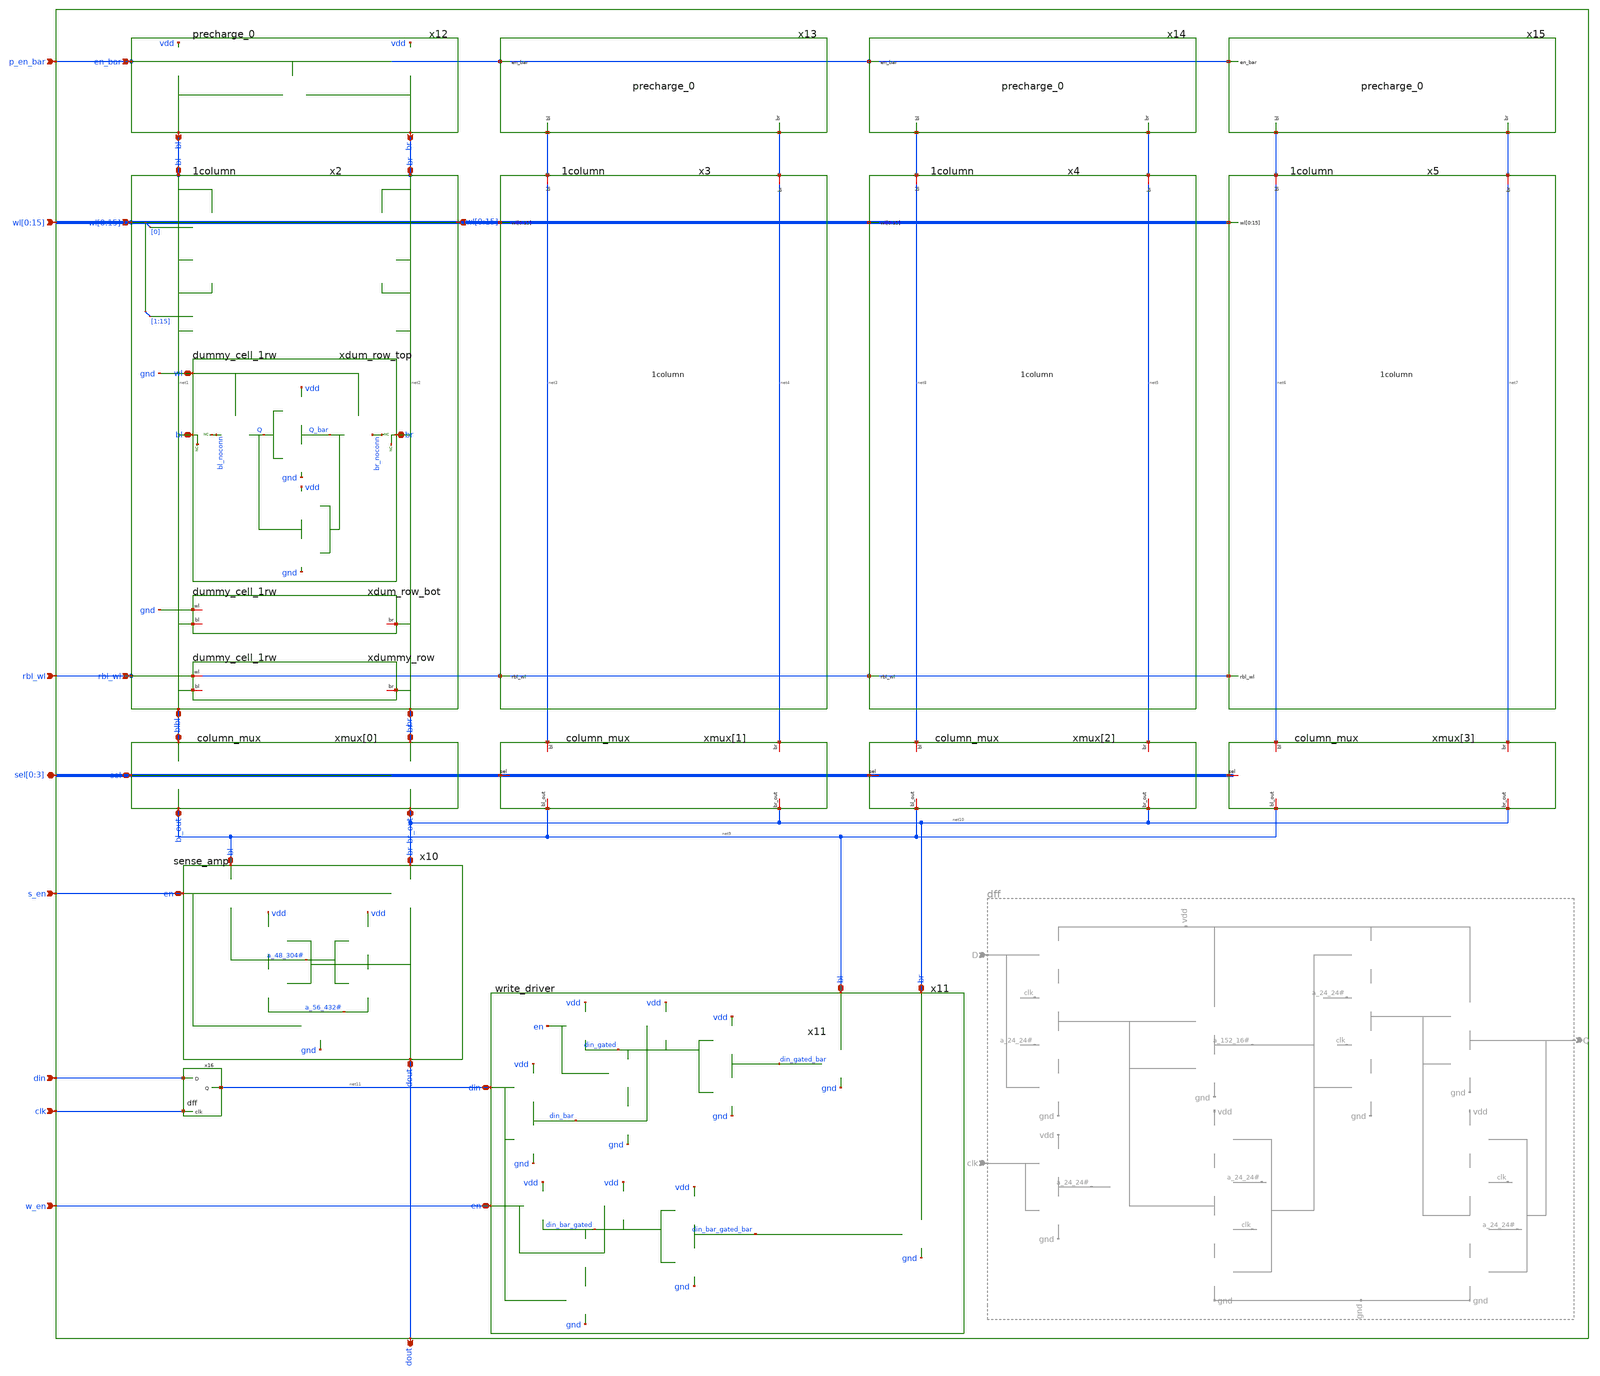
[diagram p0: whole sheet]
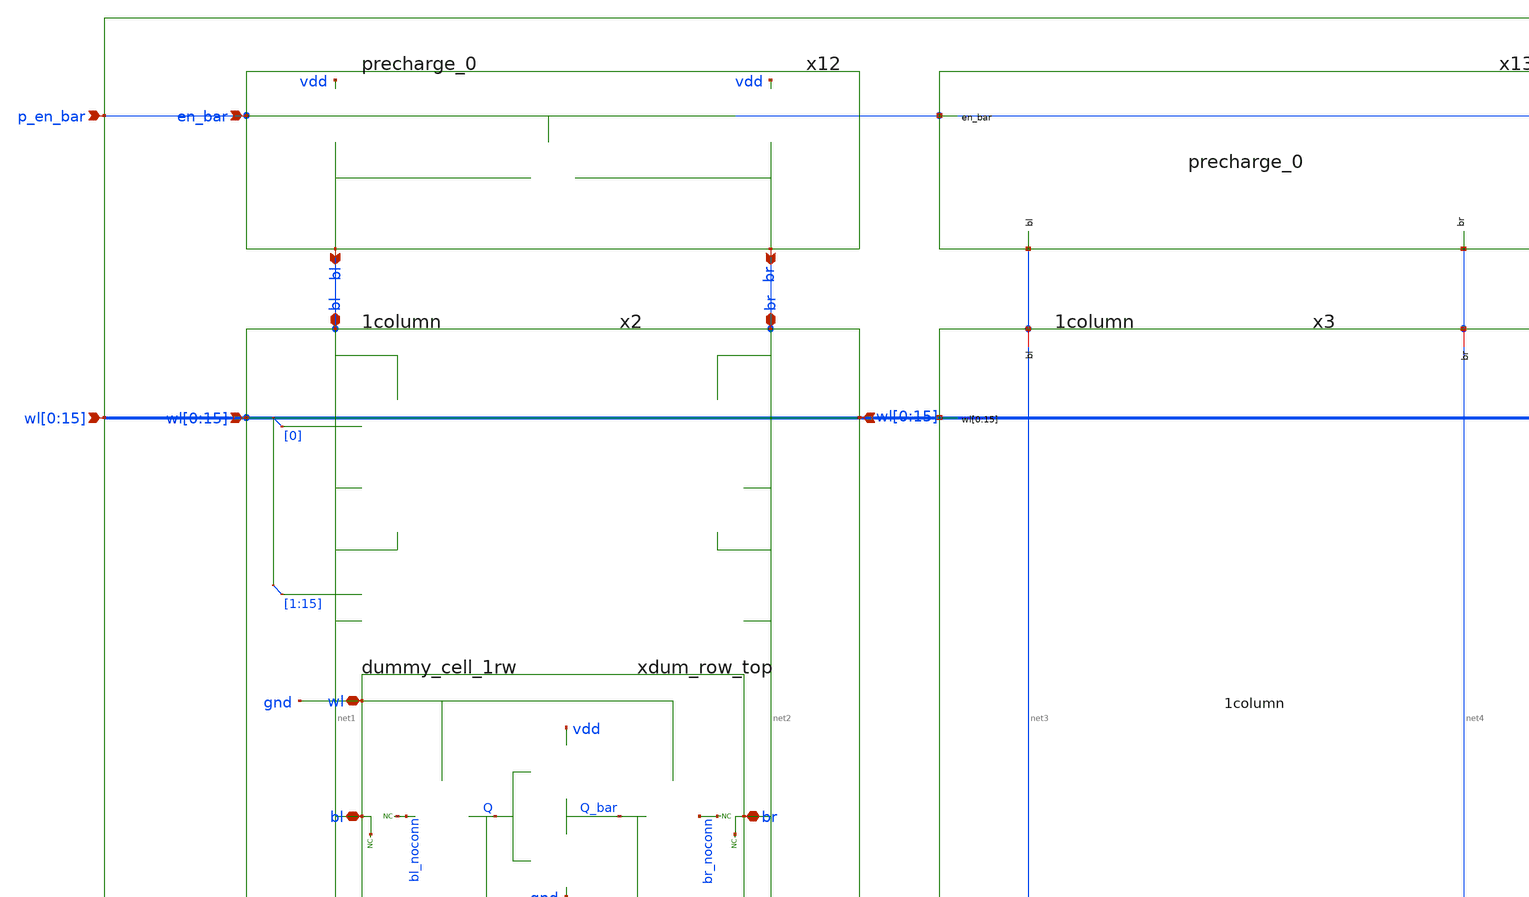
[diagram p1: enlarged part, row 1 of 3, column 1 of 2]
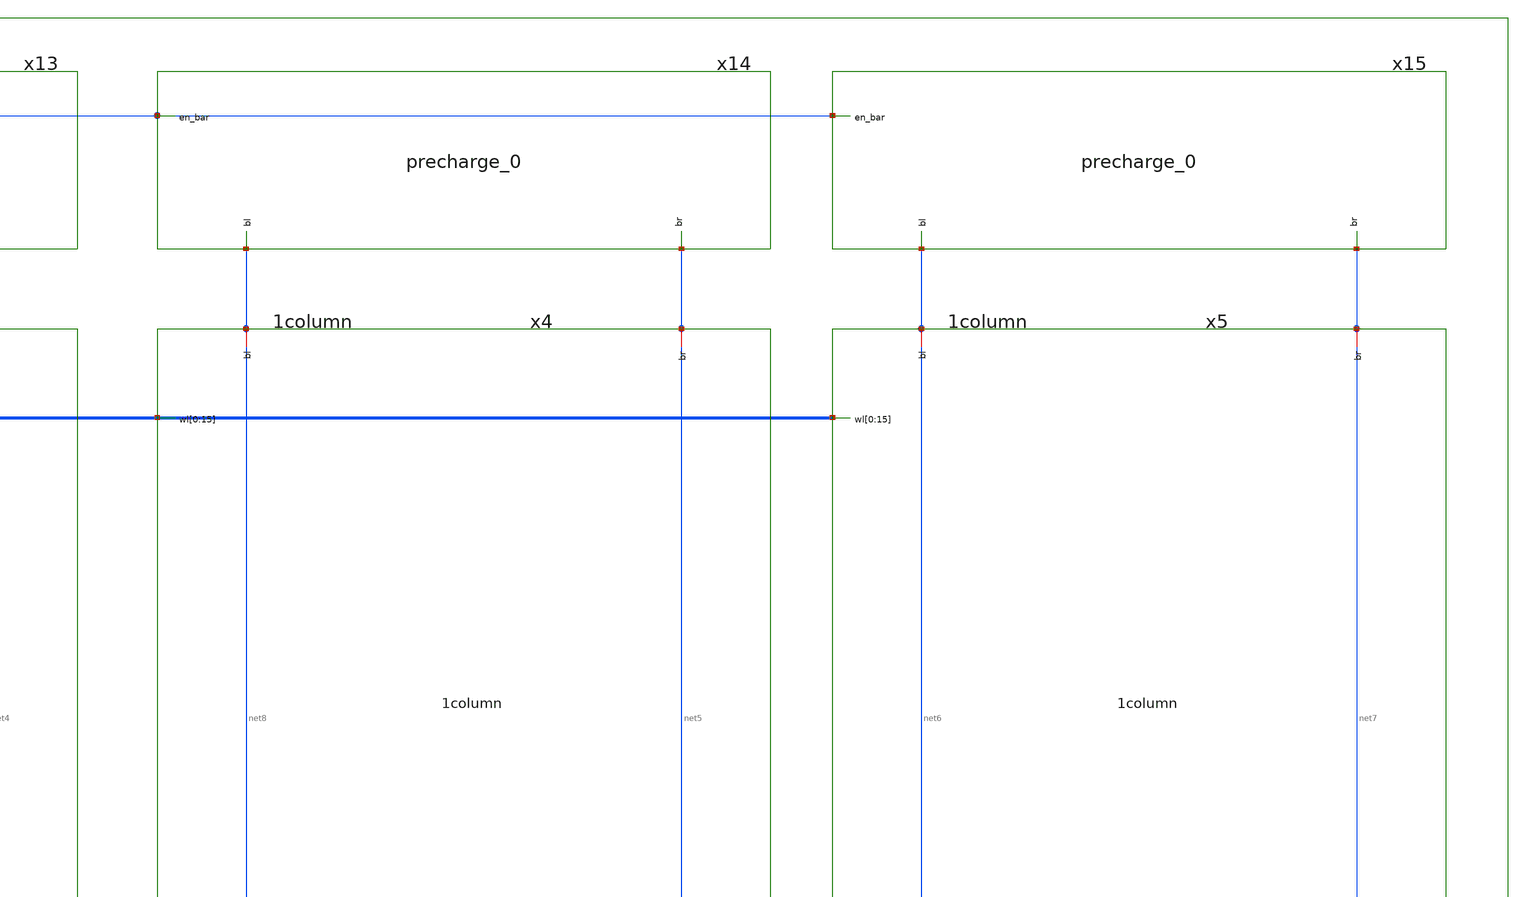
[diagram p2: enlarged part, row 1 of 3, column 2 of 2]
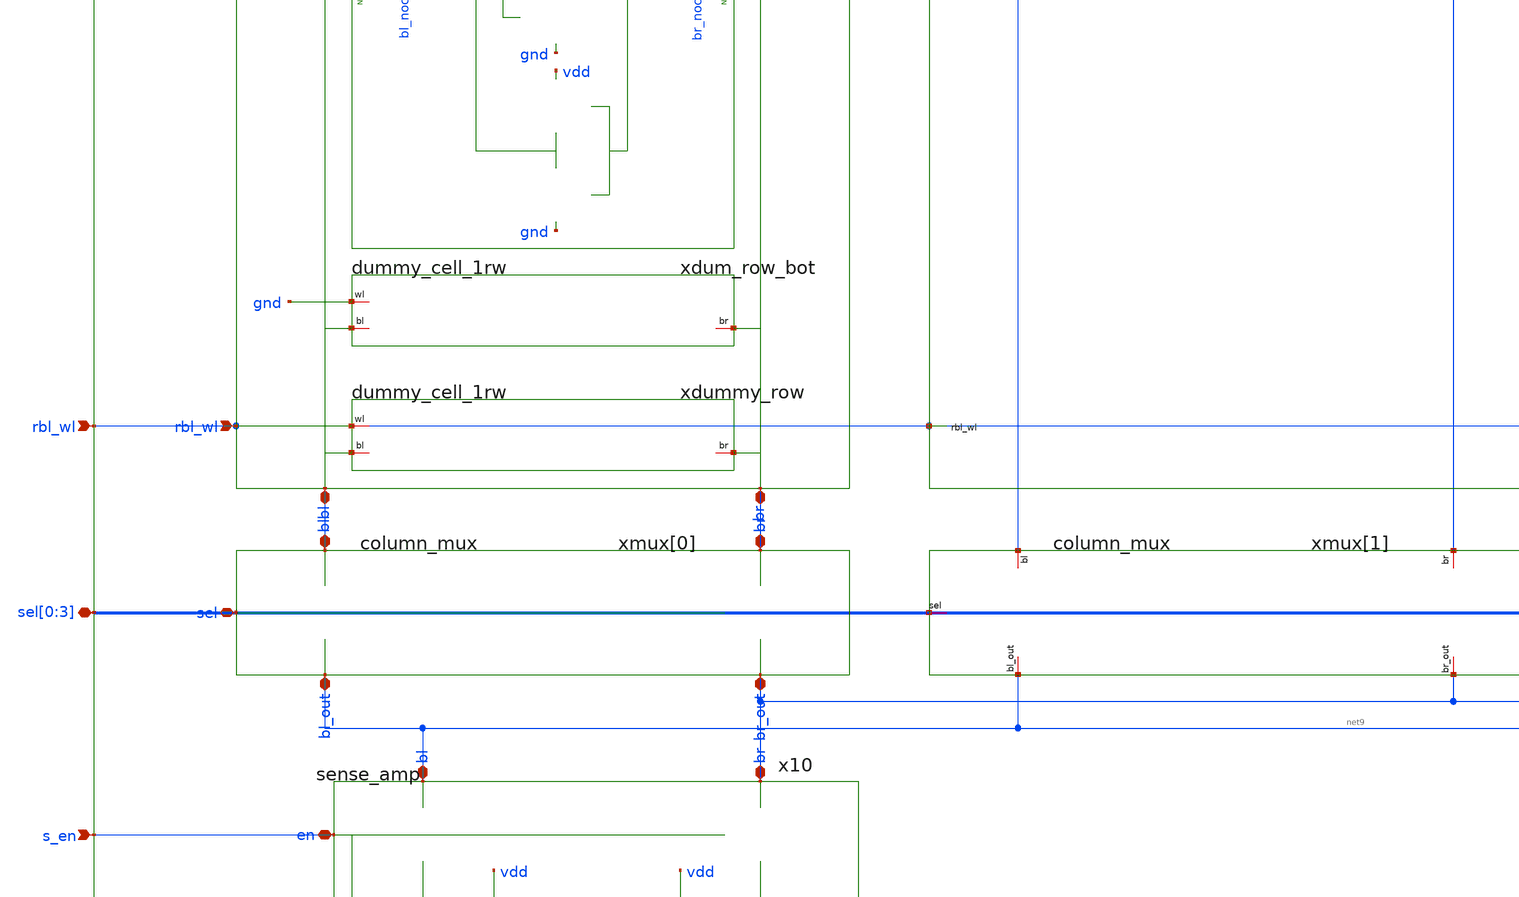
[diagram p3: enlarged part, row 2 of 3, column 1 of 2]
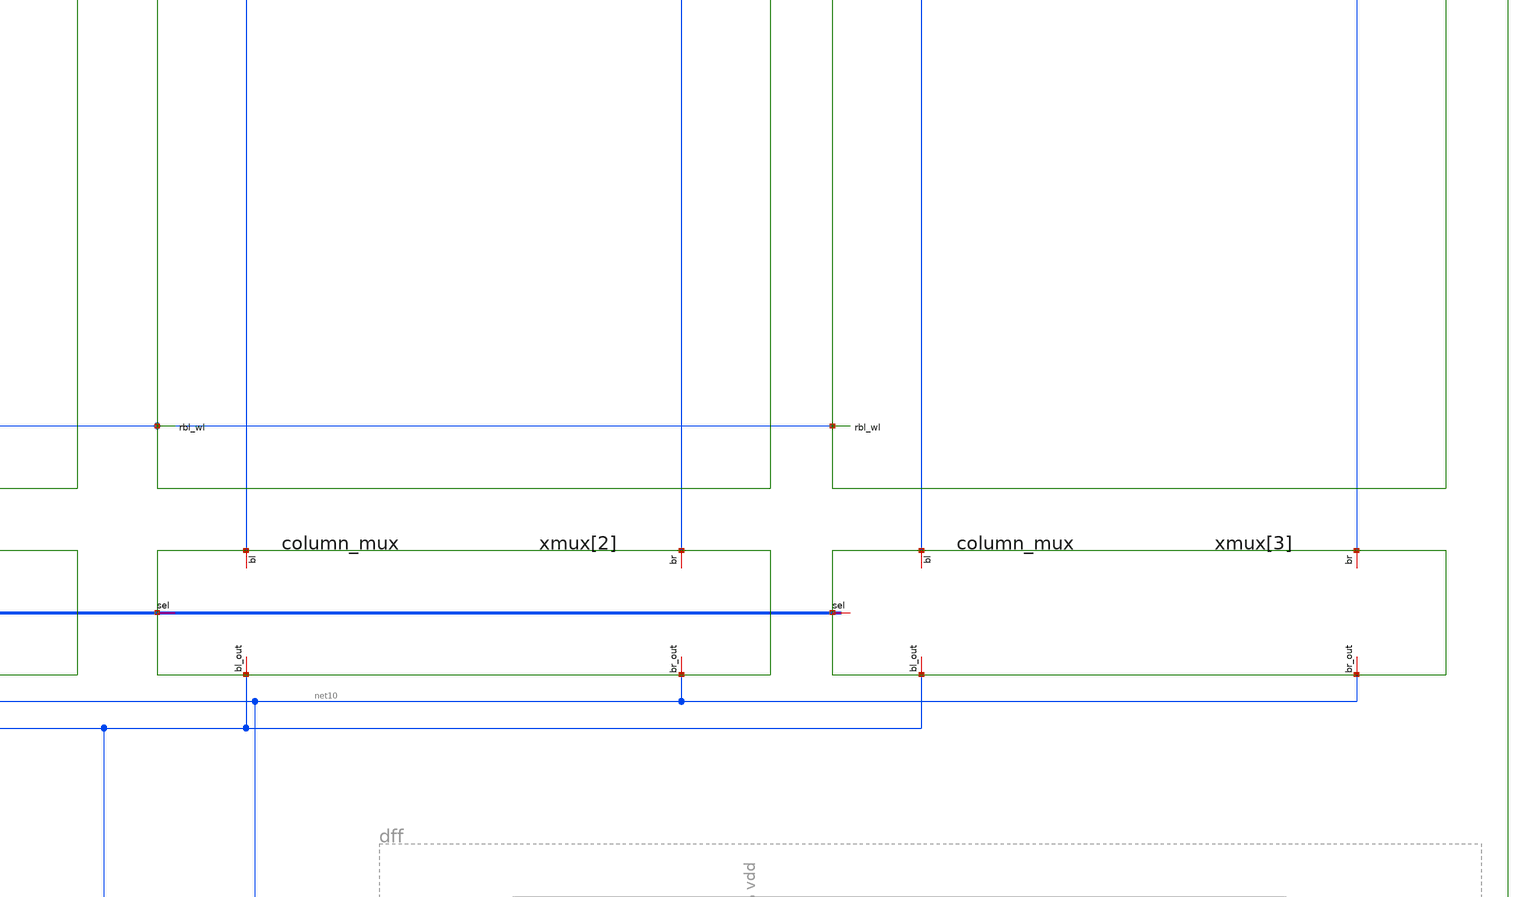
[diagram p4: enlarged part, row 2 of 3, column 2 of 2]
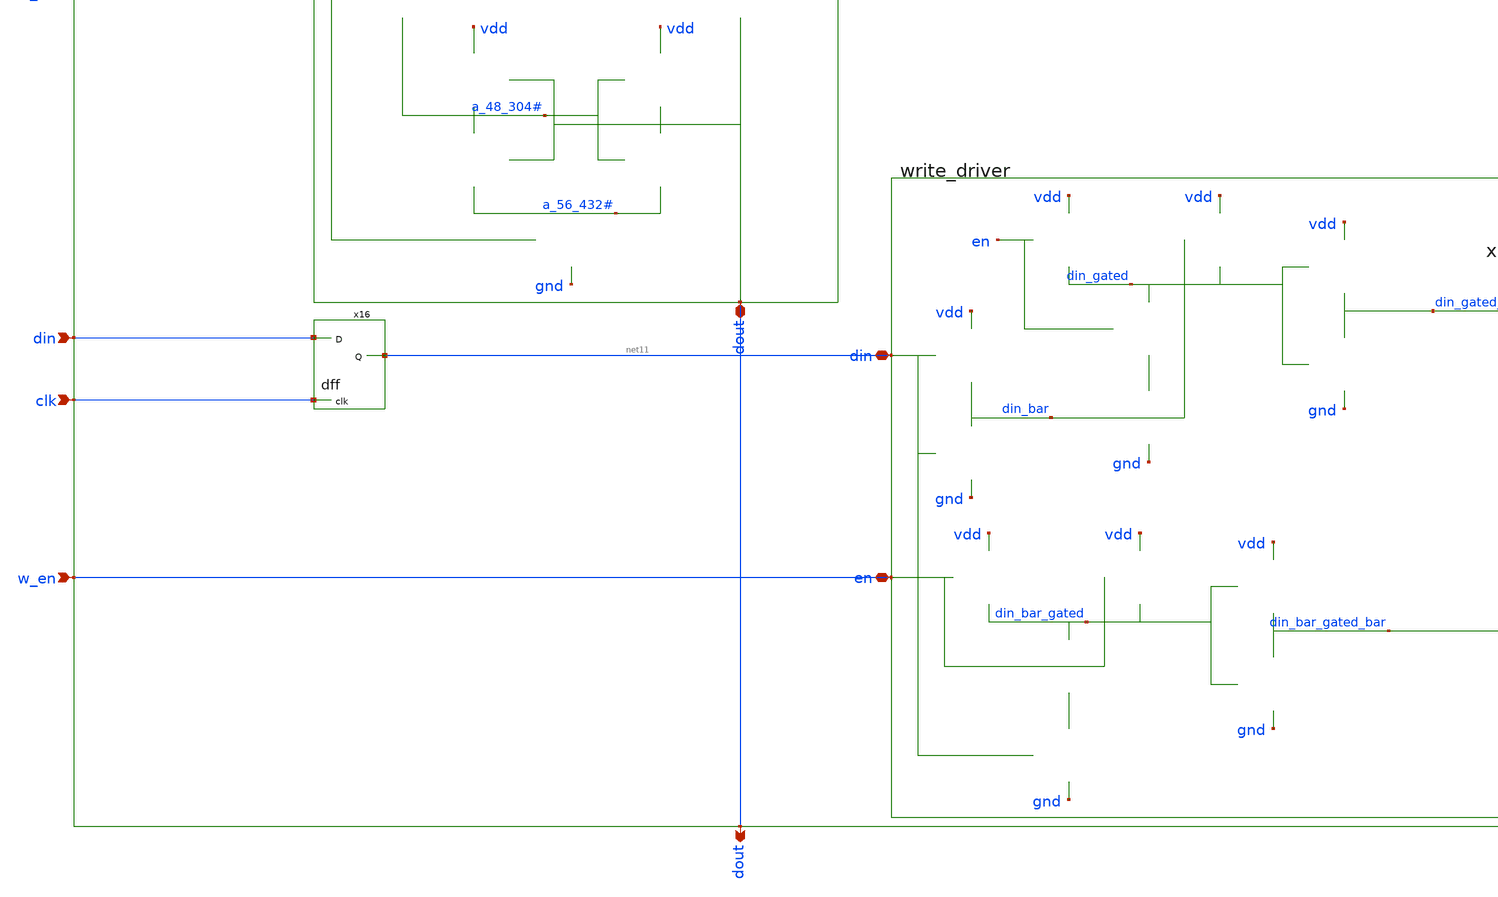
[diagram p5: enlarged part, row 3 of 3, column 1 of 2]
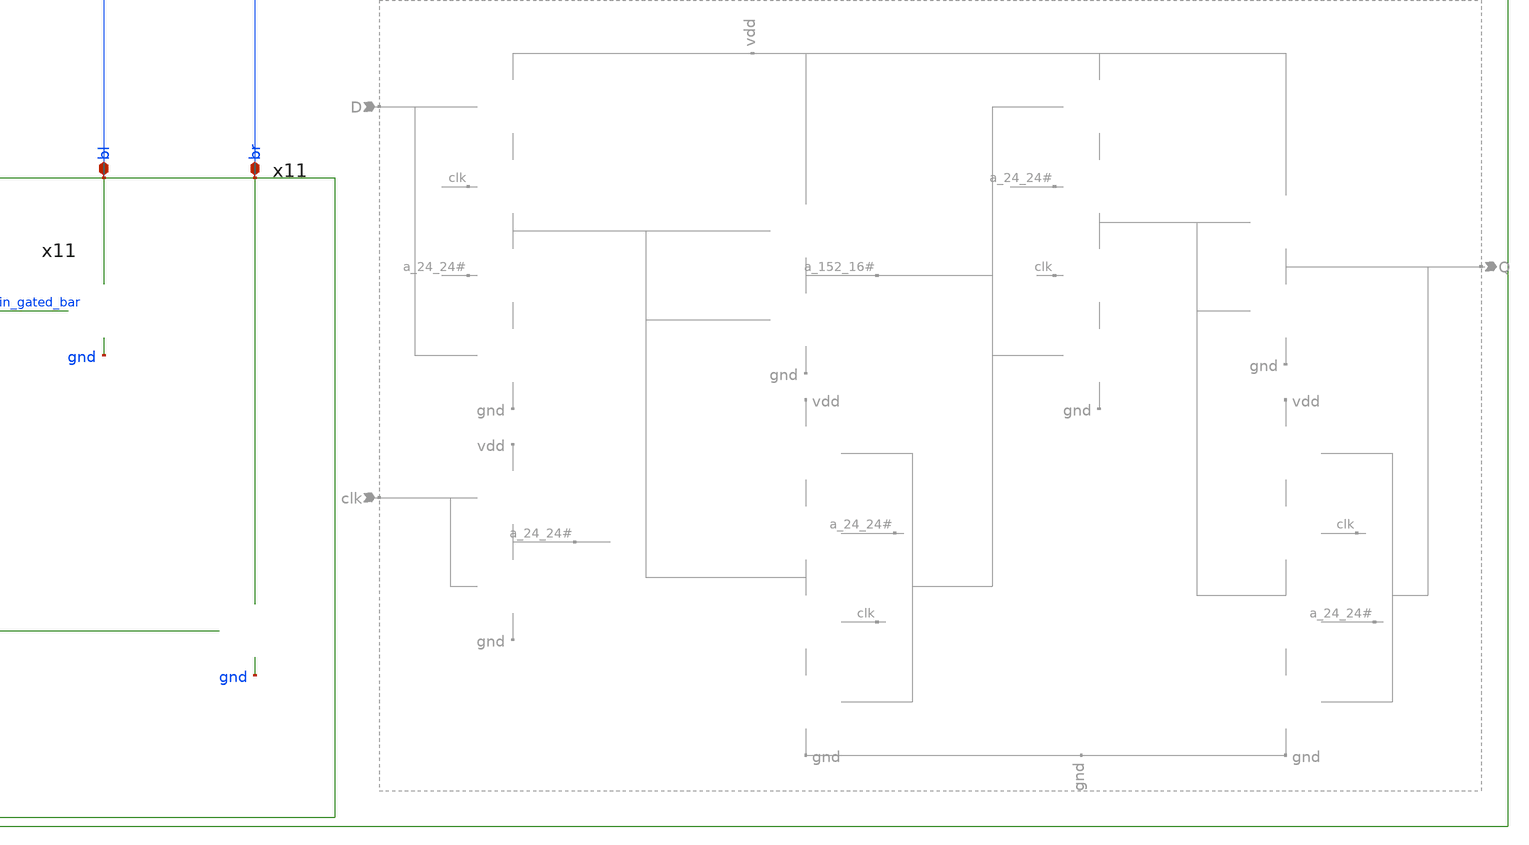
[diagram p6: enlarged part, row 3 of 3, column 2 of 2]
** sch_path: sram_2_64_scn4m_lcc/column.sch
**.subckt column dout din s_en p_en_bar w_en sel[0],sel[1],sel[2],sel[3]
*+ wl[0],wl[1],wl[2],wl[3],wl[4],wl[5],wl[6],wl[7],wl[8],wl[9],wl[10],wl[11],wl[12],wl[13],wl[14],wl[15] rbl_wl clk
*.opin dout
*.ipin din
*.ipin s_en
*.ipin p_en_bar
*.ipin w_en
*.iopin sel[0],sel[1],sel[2],sel[3]
*.ipin
*+ wl[0],wl[1],wl[2],wl[3],wl[4],wl[5],wl[6],wl[7],wl[8],wl[9],wl[10],wl[11],wl[12],wl[13],wl[14],wl[15]
*.ipin rbl_wl
*.ipin clk
x2 net1 net2 rbl_wl wl[0] wl[1] wl[2] wl[3] wl[4] wl[5] wl[6] wl[7] wl[8] wl[9] wl[10] wl[11] wl[12]
+ wl[13] wl[14] wl[15] vdd gnd 1column
x4 net5 net8 wl[0] wl[1] wl[2] wl[3] wl[4] wl[5] wl[6] wl[7] wl[8] wl[9] wl[10] wl[11] wl[12] wl[13]
+ wl[14] wl[15] rbl_wl vdd gnd 1column
x5 net7 net6 wl[0] wl[1] wl[2] wl[3] wl[4] wl[5] wl[6] wl[7] wl[8] wl[9] wl[10] wl[11] wl[12] wl[13]
+ wl[14] wl[15] rbl_wl vdd gnd 1column
xmux[0] net1 net2 sel[0] net9 net10 vdd gnd column_mux
xmux[1] net3 net4 sel[0] net9 net10 vdd gnd column_mux
xmux[2] net8 net5 sel[0] net9 net10 vdd gnd column_mux
xmux[3] net6 net7 sel[0] net9 net10 vdd gnd column_mux
x10 net9 net10 dout s_en vdd gnd sense_amp
x11 net11 net9 net10 w_en vdd gnd write_driver
x12 net1 net2 p_en_bar vdd precharge_0
x13 net3 net4 p_en_bar vdd precharge_0
x14 net8 net5 p_en_bar vdd precharge_0
x15 net6 net7 p_en_bar vdd precharge_0
x16 din net11 clk vdd gnd dff
x3 net4 net3 wl[0] wl[1] wl[2] wl[3] wl[4] wl[5] wl[6] wl[7] wl[8] wl[9] wl[10] wl[11] wl[12] wl[13]
+ wl[14] wl[15] rbl_wl vdd gnd 1column
**.ends
.end
